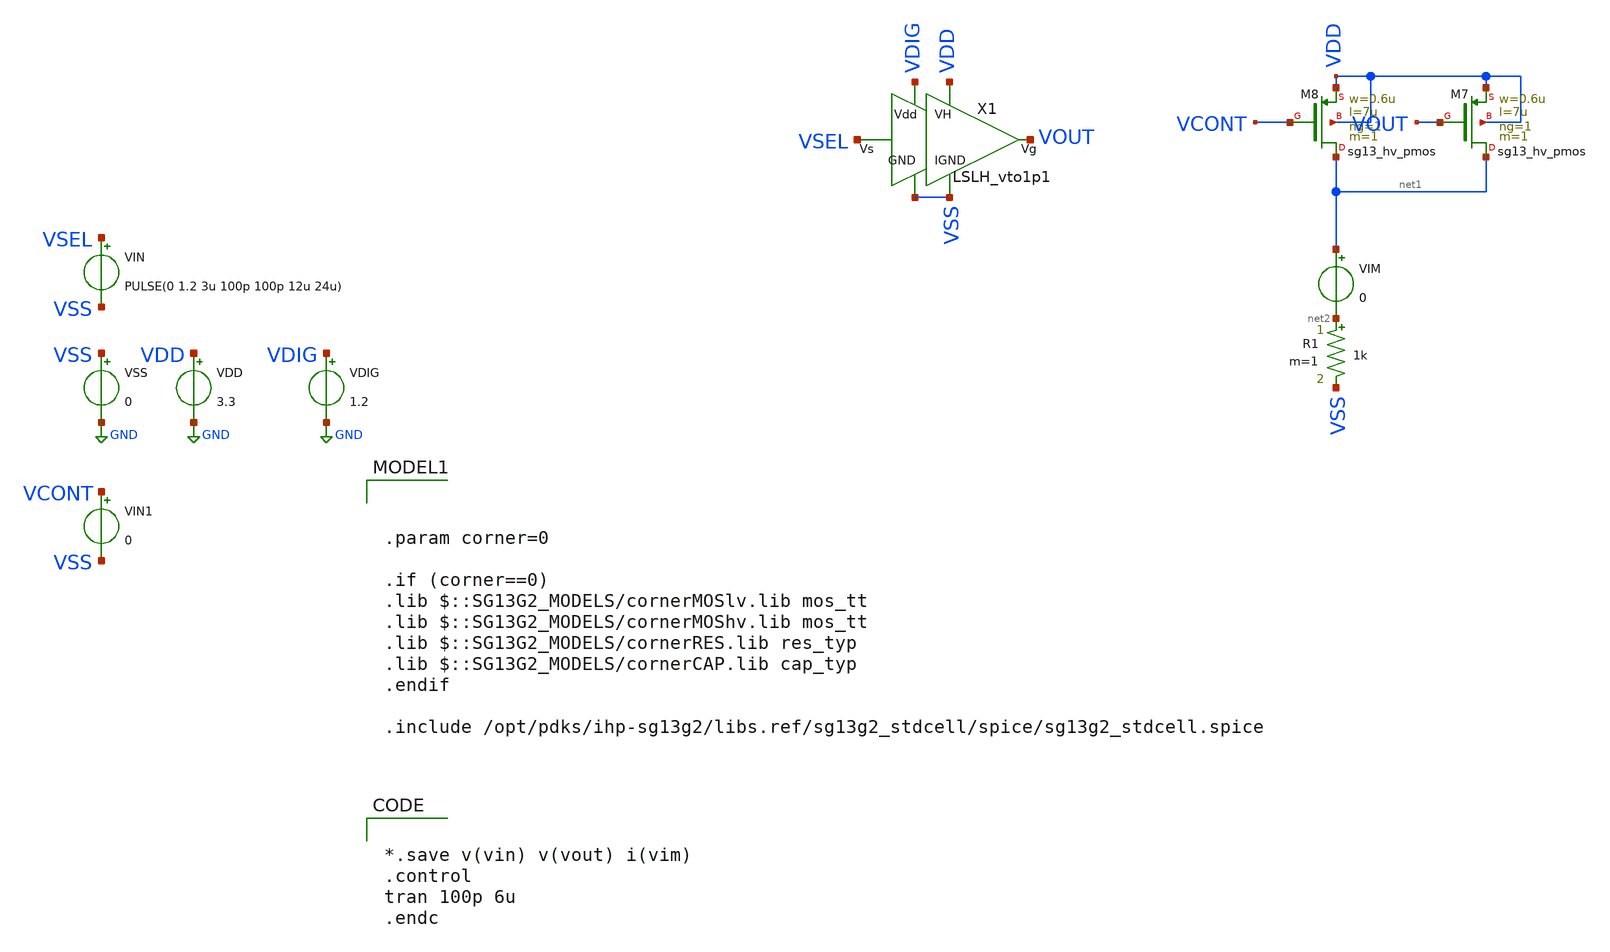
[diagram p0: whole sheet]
** sch_path: ChipUSM_AnalogTrack24/LSLH/tb_LSLH_vto1p1.sch
**.subckt tb_LSLH_vto1p1
VDD VDD GND 3.3
VSS VSS GND 0
VIN VSEL VSS PULSE(0 1.2 3u 100p 100p 12u 24u)
VIN1 VCONT VSS 0
XM8 net1 VCONT VDD VDD sg13_hv_pmos w=0.6u l=7u ng=1 m=1 mm_ok=1
XM7 net1 VOUT VDD VDD sg13_hv_pmos w=0.6u l=7u ng=1 m=1 mm_ok=1
R1 net2 VSS 1k m=1
VIM net1 net2 0
X1 VSEL VOUT VDIG VDD VSS VSS LSLH_vto1p1
VDIG VDIG GND 1.2
**** begin user architecture code


*.save v(vin) v(vout) i(vim)
.control
tran 100p 6u
.endc




.param corner=0

.if (corner==0)
.lib $::SG13G2_MODELS/cornerMOSlv.lib mos_tt
.lib $::SG13G2_MODELS/cornerMOShv.lib mos_tt
.lib $::SG13G2_MODELS/cornerRES.lib res_typ
.lib $::SG13G2_MODELS/cornerCAP.lib cap_typ
.endif

.include /opt/pdks/ihp-sg13g2/libs.ref/sg13g2_stdcell/spice/sg13g2_stdcell.spice

**** end user architecture code
**.ends

* expanding   symbol:  ./LSLH_vto1p1.sym # of pins=6
** sym_path: ChipUSM_AnalogTrack24/LSLH/LSLH_vto1p1.sym
** sch_path: ChipUSM_AnalogTrack24/LSLH/LSLH_vto1p1.sch
.subckt LSLH_vto1p1 Vs Vg Vdd VH GND IGND
*.iopin VH
*.iopin Vdd
*.ipin Vs
*.opin Vg
*.iopin GND
*.iopin IGND
XMD9 VgMD2 Vs Vdd Vdd sg13_lv_pmos w=1.12u l=0.13u ng=1 m=2 mm_ok=1
XMD10 GND Vs VgMD2 GND sg13_lv_nmos w=1.12u l=0.13u ng=1 m=2 mm_ok=1
XMD1 Vg VgMD1 VH VH sg13_hv_pmos w=10u l=0.4u ng=1 m=1 mm_ok=1
XMD3 VgMD1 Vg VH VH sg13_hv_pmos w=10u l=0.4u ng=1 m=1 mm_ok=1
XMD2 IGND VgMD2 Vg IGND sg13_hv_nmos w=10u l=0.45u ng=1 m=6 mm_ok=1
XMD4 IGND Vs VgMD1 IGND sg13_hv_nmos w=10u l=0.45u ng=1 m=6 mm_ok=1
.ends

.GLOBAL GND
.end
